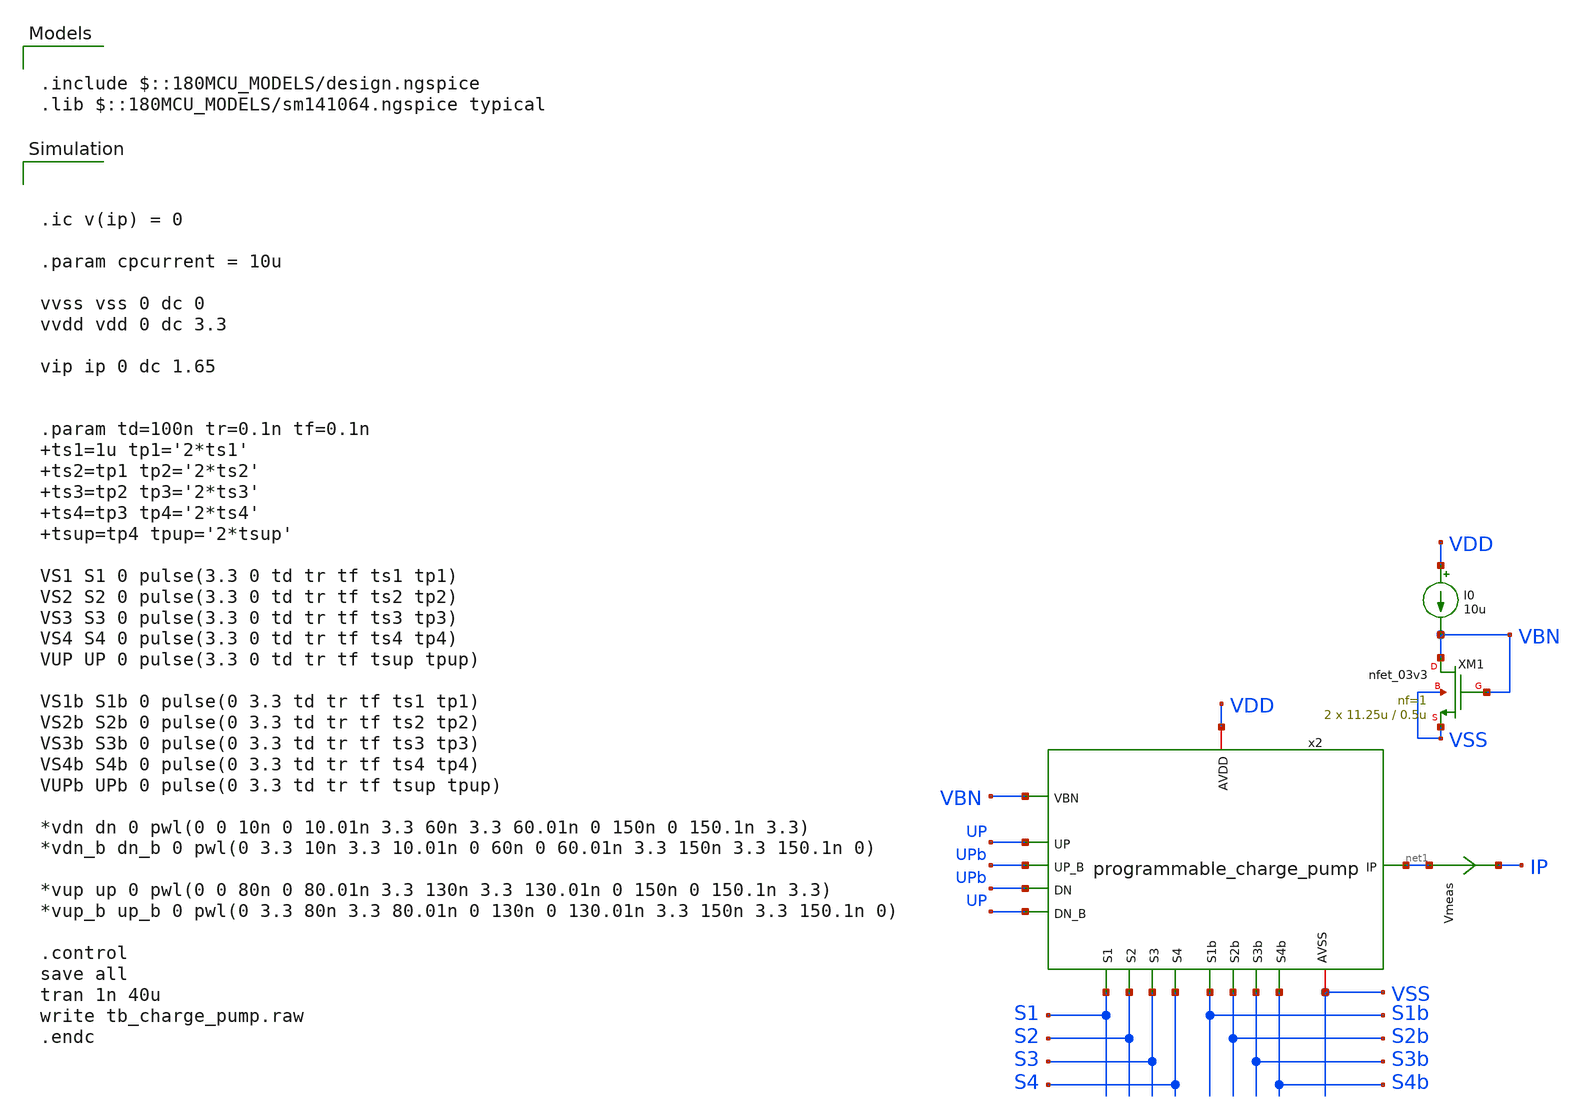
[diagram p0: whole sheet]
** sch_path: designs/libs/tb_analog/tb_programmable_charge_pump/tb_programmable_charge_pump.sch
**.subckt tb_programmable_charge_pump
Vmeas net1 IP 0
.save i(vmeas)
XM1 VBN VBN VSS VSS nfet_03v3 L=0.5u W=11.25u nf=1 ad='int((nf+1)/2) * W/nf * 0.18u' as='int((nf+2)/2) * W/nf * 0.18u'
+ pd='2*int((nf+1)/2) * (W/nf + 0.18u)' ps='2*int((nf+2)/2) * (W/nf + 0.18u)' nrd='0.18u / W' nrs='0.18u / W'
+ sa=0 sb=0 sd=0 m=2
I0 VDD VBN 10u
x2 VSS VDD UP UPb UPb net1 UP VBN S1b S1 S2b S2 S3b S3 S4b S4 programmable_charge_pump
**** begin user architecture code



.ic v(ip) = 0

.param cpcurrent = 10u

vvss vss 0 dc 0
vvdd vdd 0 dc 3.3

vip ip 0 dc 1.65


.param td=100n tr=0.1n tf=0.1n ts1=1u tp1='2*ts1' ts2=tp1 tp2='2*ts2' ts3=tp2 tp3='2*ts3' ts4=tp3 tp4='2*ts4'
+ tsup=tp4 tpup='2*tsup'

VS1 S1 0 pulse(3.3 0 td tr tf ts1 tp1)
VS2 S2 0 pulse(3.3 0 td tr tf ts2 tp2)
VS3 S3 0 pulse(3.3 0 td tr tf ts3 tp3)
VS4 S4 0 pulse(3.3 0 td tr tf ts4 tp4)
VUP UP 0 pulse(3.3 0 td tr tf tsup tpup)

VS1b S1b 0 pulse(0 3.3 td tr tf ts1 tp1)
VS2b S2b 0 pulse(0 3.3 td tr tf ts2 tp2)
VS3b S3b 0 pulse(0 3.3 td tr tf ts3 tp3)
VS4b S4b 0 pulse(0 3.3 td tr tf ts4 tp4)
VUPb UPb 0 pulse(0 3.3 td tr tf tsup tpup)

*vdn dn 0 pwl(0 0 10n 0 10.01n 3.3 60n 3.3 60.01n 0 150n 0 150.1n 3.3)
*vdn_b dn_b 0 pwl(0 3.3 10n 3.3 10.01n 0 60n 0 60.01n 3.3 150n 3.3 150.1n 0)

*vup up 0 pwl(0 0 80n 0 80.01n 3.3 130n 3.3 130.01n 0 150n 0 150.1n 3.3)
*vup_b up_b 0 pwl(0 3.3 80n 3.3 80.01n 0 130n 0 130.01n 3.3 150n 3.3 150.1n 0)

.control
save all
tran 1n 40u
write tb_charge_pump.raw
.endc



.include $::180MCU_MODELS/design.ngspice
.lib $::180MCU_MODELS/sm141064.ngspice typical

**** end user architecture code
**.ends

* expanding   symbol:  libs/core_analog/programmable_charge_pump/programmable_charge_pump.sym # of
*+ pins=16
** sym_path: designs/libs/core_analog/programmable_charge_pump/programmable_charge_pump.sym
** sch_path: designs/libs/core_analog/programmable_charge_pump/programmable_charge_pump.sch
.subckt programmable_charge_pump AVSS AVDD UP UP_B DN IP DN_B VBN S1b S1 S2b S2 S3b S3 S4b S4
*.ipin VBN
*.ipin S1b
*.ipin S1
*.ipin S2b
*.ipin S2
*.ipin S3b
*.ipin S3
*.ipin S4b
*.ipin S4
*.iopin AVSS
*.iopin AVDD
*.ipin UP
*.ipin UP_B
*.ipin DN
*.ipin DN_B
*.opin IP
x1 AVDD AVSS UP UP_B DN DN_B VBN1 IP S1b charge_pump
x61 AVDD AVSS UP UP_B DN DN_B VBN2 IP S2b charge_pump
x62 AVDD AVSS UP UP_B DN DN_B VBN2 IP S2b charge_pump
x71 AVDD AVSS UP UP_B DN DN_B VBN3 IP S3b charge_pump
x72 AVDD AVSS UP UP_B DN DN_B VBN3 IP S3b charge_pump
x73 AVDD AVSS UP UP_B DN DN_B VBN3 IP S3b charge_pump
x74 AVDD AVSS UP UP_B DN DN_B VBN3 IP S3b charge_pump
x81 AVDD AVSS UP UP_B DN DN_B VBN4 IP S4b charge_pump
x82 AVDD AVSS UP UP_B DN DN_B VBN4 IP S4b charge_pump
x83 AVDD AVSS UP UP_B DN DN_B VBN4 IP S4b charge_pump
x84 AVDD AVSS UP UP_B DN DN_B VBN4 IP S4b charge_pump
x85 AVDD AVSS UP UP_B DN DN_B VBN4 IP S4b charge_pump
x86 AVDD AVSS UP UP_B DN DN_B VBN4 IP S4b charge_pump
x87 AVDD AVSS UP UP_B DN DN_B VBN4 IP S4b charge_pump
x88 AVDD AVSS UP UP_B DN DN_B VBN4 IP S4b charge_pump
x2 VBN AVSS S1 VBN1 S1b AVDD transmission_gate
x0 AVDD AVSS UP UP_B DN DN_B VBN IP AVSS charge_pump
x3 VBN AVSS S2 VBN2 S2b AVDD transmission_gate
x4 VBN AVSS S3 VBN3 S3b AVDD transmission_gate
x5 VBN AVSS S4 VBN4 S4b AVDD transmission_gate
.ends


* expanding   symbol:  libs/core_analog/charge_pump/charge_pump.sym # of pins=9
** sym_path: designs/libs/core_analog/charge_pump/charge_pump.sym
** sch_path: designs/libs/core_analog/charge_pump/charge_pump.sch
.subckt charge_pump VDD VSS UP UP_B DN DN_B VBN IP S
*.iopin VDD
*.iopin VSS
*.ipin UP
*.ipin UP_B
*.ipin DN
*.ipin DN_B
*.ipin VBN
*.iopin IP
*.ipin S
x1 net5 net5 VDD net5 VDD cp_sym_load
x2 net3 net3 VDD net3 VDD cp_sym_load
x3 net4 net4 VDD net4 VDD cp_sym_load
x4 net5 net5 VDD IP VDD cp_sym_load
XM1 net1 VBN VSS VSS nfet_03v3 L=0.5u W=11.25u nf=1 ad='int((nf+1)/2) * W/nf * 0.18u' as='int((nf+2)/2) * W/nf * 0.18u'
+ pd='2*int((nf+1)/2) * (W/nf + 0.18u)' ps='2*int((nf+2)/2) * (W/nf + 0.18u)' nrd='0.18u / W' nrs='0.18u / W'
+ sa=0 sb=0 sd=0 m=1
XM3 net5 DN net1 VSS nfet_03v3 L=0.5u W=2.08u nf=1 ad='int((nf+1)/2) * W/nf * 0.18u' as='int((nf+2)/2) * W/nf * 0.18u'
+ pd='2*int((nf+1)/2) * (W/nf + 0.18u)' ps='2*int((nf+2)/2) * (W/nf + 0.18u)' nrd='0.18u / W' nrs='0.18u / W'
+ sa=0 sb=0 sd=0 m=1
XM4 net3 DN_B net1 VSS nfet_03v3 L=0.5u W=2.08u nf=1 ad='int((nf+1)/2) * W/nf * 0.18u' as='int((nf+2)/2) * W/nf * 0.18u'
+ pd='2*int((nf+1)/2) * (W/nf + 0.18u)' ps='2*int((nf+2)/2) * (W/nf + 0.18u)' nrd='0.18u / W' nrs='0.18u / W'
+ sa=0 sb=0 sd=0 m=1
XM5 net4 UP_B net2 VSS nfet_03v3 L=0.5u W=2.08u nf=1 ad='int((nf+1)/2) * W/nf * 0.18u' as='int((nf+2)/2) * W/nf * 0.18u'
+ pd='2*int((nf+1)/2) * (W/nf + 0.18u)' ps='2*int((nf+2)/2) * (W/nf + 0.18u)' nrd='0.18u / W' nrs='0.18u / W'
+ sa=0 sb=0 sd=0 m=1
XM6 IP UP net2 VSS nfet_03v3 L=0.5u W=2.08u nf=1 ad='int((nf+1)/2) * W/nf * 0.18u' as='int((nf+2)/2) * W/nf * 0.18u'
+ pd='2*int((nf+1)/2) * (W/nf + 0.18u)' ps='2*int((nf+2)/2) * (W/nf + 0.18u)' nrd='0.18u / W' nrs='0.18u / W'
+ sa=0 sb=0 sd=0 m=1
XM2 net2 VBN VSS VSS nfet_03v3 L=0.5u W=11.25u nf=1 ad='int((nf+1)/2) * W/nf * 0.18u' as='int((nf+2)/2) * W/nf * 0.18u'
+ pd='2*int((nf+1)/2) * (W/nf + 0.18u)' ps='2*int((nf+2)/2) * (W/nf + 0.18u)' nrd='0.18u / W' nrs='0.18u / W'
+ sa=0 sb=0 sd=0 m=1
XM7 VBN S VSS VSS nfet_03v3 L=0.5u W=1u nf=1 ad='int((nf+1)/2) * W/nf * 0.18u' as='int((nf+2)/2) * W/nf * 0.18u'
+ pd='2*int((nf+1)/2) * (W/nf + 0.18u)' ps='2*int((nf+2)/2) * (W/nf + 0.18u)' nrd='0.18u / W' nrs='0.18u / W'
+ sa=0 sb=0 sd=0 m=1
XM8 VBN S VSS VSS nfet_03v3 L=0.5u W=1u nf=1 ad='int((nf+1)/2) * W/nf * 0.18u' as='int((nf+2)/2) * W/nf * 0.18u'
+ pd='2*int((nf+1)/2) * (W/nf + 0.18u)' ps='2*int((nf+2)/2) * (W/nf + 0.18u)' nrd='0.18u / W' nrs='0.18u / W'
+ sa=0 sb=0 sd=0 m=1
.ends


* expanding   symbol:  libs/core_analog/transmission_gate/transmission_gate.sym # of pins=6
** sym_path: designs/libs/core_analog/transmission_gate/transmission_gate.sym
** sch_path: designs/libs/core_analog/transmission_gate/transmission_gate.sch
.subckt transmission_gate ind vss clkn ins clkp vdd
*.iopin ind
*.iopin ins
*.iopin clkn
*.iopin clkp
*.iopin vdd
*.iopin vss
XM1 ind clkp ins vdd pfet_03v3 L=0.5u W=3.0u nf=1 ad='int((nf+1)/2) * W/nf * 0.18u' as='int((nf+2)/2) * W/nf * 0.18u'
+ pd='2*int((nf+1)/2) * (W/nf + 0.18u)' ps='2*int((nf+2)/2) * (W/nf + 0.18u)' nrd='0.18u / W' nrs='0.18u / W'
+ sa=0 sb=0 sd=0 m=1
XM2 ind clkn ins vss nfet_03v3 L=0.5u W=1.0u nf=1 ad='int((nf+1)/2) * W/nf * 0.18u' as='int((nf+2)/2) * W/nf * 0.18u'
+ pd='2*int((nf+1)/2) * (W/nf + 0.18u)' ps='2*int((nf+2)/2) * (W/nf + 0.18u)' nrd='0.18u / W' nrs='0.18u / W'
+ sa=0 sb=0 sd=0 m=1
.ends


* expanding   symbol:  libs/core_analog/cp_sym_load/cp_sym_load.sym # of pins=5
** sym_path: designs/libs/core_analog/cp_sym_load/cp_sym_load.sym
** sch_path: designs/libs/core_analog/cp_sym_load/cp_sym_load.sch
.subckt cp_sym_load G1 G2 S D VDD
*.ipin G1
*.ipin G2
*.iopin S
*.iopin D
*.iopin VDD
XM1 D G1 S VDD pfet_03v3 L=1.5u W=1.1u nf=1 ad='int((nf+1)/2) * W/nf * 0.18u' as='int((nf+2)/2) * W/nf * 0.18u'
+ pd='2*int((nf+1)/2) * (W/nf + 0.18u)' ps='2*int((nf+2)/2) * (W/nf + 0.18u)' nrd='0.18u / W' nrs='0.18u / W'
+ sa=0 sb=0 sd=0 m=1
XM2 D G2 S VDD pfet_03v3 L=1.5u W=1.1u nf=1 ad='int((nf+1)/2) * W/nf * 0.18u' as='int((nf+2)/2) * W/nf * 0.18u'
+ pd='2*int((nf+1)/2) * (W/nf + 0.18u)' ps='2*int((nf+2)/2) * (W/nf + 0.18u)' nrd='0.18u / W' nrs='0.18u / W'
+ sa=0 sb=0 sd=0 m=1
.ends

.end
